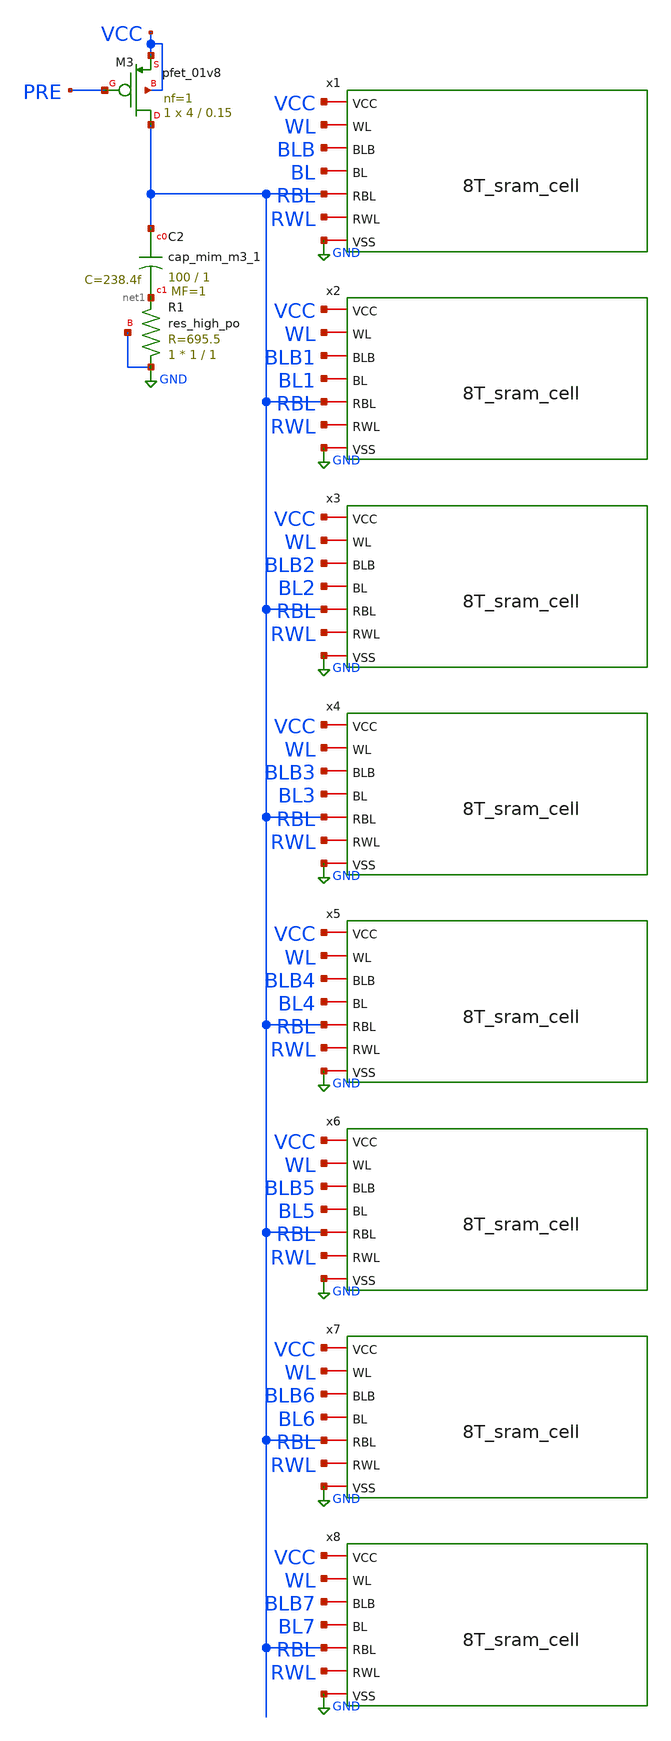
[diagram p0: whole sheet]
** sch_path: vscode/8T_sram_array_test - Copy.sch
**.subckt 8T_sram_array_test - Copy
x1 VCC WL BLB BL RBL RWL GND 8T_sram_cell
XC2 RBL net1 sky130_fd_pr__cap_mim_m3_1 W=100 L=1 MF=1 m=1
XM3 RBL PRE VCC VCC sky130_fd_pr__pfet_01v8 L=0.15 W=4 nf=1 ad='int((1 + 1)/2) * 4 / 1 * 0.29' as='int((1 + 2)/2) * 4 / 1 * 0.29'
+ pd='2*int((1 + 1)/2) * (4 / 1 + 0.29)' ps='2*int((1 + 2)/2) * (4 / 1 + 0.29)' nrd='0.29 / 4 ' nrs='0.29 / 4 '
+ sa=0 sb=0 sd=0 mult=1 m=1
XR1 GND net1 GND sky130_fd_pr__res_high_po W=1 L=1 mult=1 m=1
x2 VCC WL BLB1 BL1 RBL RWL GND 8T_sram_cell
x3 VCC WL BLB2 BL2 RBL RWL GND 8T_sram_cell
x4 VCC WL BLB3 BL3 RBL RWL GND 8T_sram_cell
x5 VCC WL BLB4 BL4 RBL RWL GND 8T_sram_cell
x6 VCC WL BLB5 BL5 RBL RWL GND 8T_sram_cell
x7 VCC WL BLB6 BL6 RBL RWL GND 8T_sram_cell
x8 VCC WL BLB7 BL7 RBL RWL GND 8T_sram_cell
**** begin user architecture code

** opencircuitdesign pdks install
.lib $::SKYWATER_MODELS/sky130.lib.spice tt



.param dly=0ns t_dly=2ns raise=10ps fall=10ps BL_period=20ns prds=128 pre_time=2ns read_time=0.5ns
.param VCC=1.8 VSS=0

V_VCC VCC 0 DC 1.8
V_VSS VSS 0 DC 0
**vss vss 0 DC 0
* PULSE(VSS 1.8 2ns 100ps 100ps 3ns 5ns 4)PULSE(0 1.7 {dly + t_dly/2} {raise} {fall} {(BL_period/2)- t_dly}
*+ {BL_period/2} {prds*2})

V_WL WL 0 PULSE({VSS} {VCC} {dly + t_dly/2} {raise} {fall} {(BL_period/2)- t_dly} {BL_period} {prds*2})


V_BL BLB 0 PULSE({VSS} {VCC} {dly} {raise} {fall} {BL_period} {BL_period*2} {prds})
V_BLB BL 0 PULSE({VCC} {VSS} {dly} {raise} {fall} {BL_period} {BL_period*2} {prds})

V_BL1 BLB1 0 PULSE({VSS} {VCC} {dly} {raise} {fall} {BL_period*2} {BL_period*4} {prds})
V_BLB1 BL1 0 PULSE({VCC} {VSS} {dly} {raise} {fall} {BL_period*2} {BL_period*4} {prds})

V_BL2 BLB2 0 PULSE({VSS} {VCC} {dly} {raise} {fall} {BL_period*4} {BL_period*8} {prds})
V_BLB2 BL2 0 PULSE({VCC} {VSS} {dly} {raise} {fall} {BL_period*4} {BL_period*8} {prds})

V_BL3 BLB3 0 PULSE({VSS} {VCC} {dly} {raise} {fall} {BL_period*8} {BL_period*16} {prds})
V_BLB3 BL3 0 PULSE({VCC} {VSS} {dly} {raise} {fall} {BL_period*8} {BL_period*16} {prds})

V_BL4 BLB4 0 PULSE({VSS} {VCC} {dly} {raise} {fall} {BL_period*16} {BL_period*32} {prds})
V_BLB4 BL4 0 PULSE({VCC} {VSS} {dly} {raise} {fall} {BL_period*16} {BL_period*32} {prds})

V_BL5 BLB5 0 PULSE({VSS} {VCC} {dly} {raise} {fall} {BL_period*32} {BL_period*64} {prds})
V_BLB5 BL5 0 PULSE({VCC} {VSS} {dly} {raise} {fall} {BL_period*32} {BL_period*64} {prds})

V_BL6 BLB6 0 PULSE({VSS} {VCC} {dly} {raise} {fall} {BL_period*64} {BL_period*128} {prds})
V_BLB6 BL6 0 PULSE({VCC} {VSS} {dly} {raise} {fall} {BL_period*64} {BL_period*128} {prds})

V_BL7 BLB7 0 PULSE({VSS} {VCC} {dly} {raise} {fall} {BL_period*128} {BL_period*256} {prds})
V_BLB7 BL7 0 PULSE({VCC} {VSS} {dly} {raise} {fall} {BL_period*128} {BL_period*256} {prds})


V_RWL RWL 0 PULSE({VSS} {VCC} {dly + BL_period/2 + 6ns} {raise} {fall} {read_time} {BL_period} {prds*2})
V_PRE PRE 0 PULSE({VCC} {VSS} {dly + BL_period/2} {raise} {fall} {pre_time} {BL_period} {prds*2})

.tran 0.01ns 5130ns
.control
run
* plot WL BL-2 BLB-4 RWL-6 RBL-8 PRE-10
plot WL BL-2 BL1-4 BL2-6 BL3-8 RWL-10 RBL-12 PRE-14
.endc
.save V(WL) V(BL) V(BL1) V(BL2) V(BL3) V(BL4) V(BL5) V(BL6) V(BL7) V(RWL) V(RBL) V(PRE)



**** end user architecture code
**.ends

* expanding   symbol:  8T_sram_cell.sym # of pins=7
** sym_path: vscode/8T_sram_cell.sym
** sch_path: vscode/8T_sram_cell.sch
.subckt 8T_sram_cell VCC WL BLB BL RBL RWL VSS
*.iopin VCC
*.iopin BLB
*.iopin WL
*.iopin BL
*.iopin VSS
*.iopin RBL
*.iopin RWL
XM1 q_bar q VSS VSS sky130_fd_pr__nfet_01v8 L=0.15 W=1 nf=1 ad='int((1 + 1)/2) * 1 / 1 * 0.29' as='int((1 + 2)/2) * 1 / 1 * 0.29'
+ pd='2*int((1 + 1)/2) * (1 / 1 + 0.29)' ps='2*int((1 + 2)/2) * (1 / 1 + 0.29)' nrd='0.29 / 1 ' nrs='0.29 / 1 '
+ sa=0 sb=0 sd=0 mult=1 m=1
XM2 q q_bar VSS VSS sky130_fd_pr__nfet_01v8 L=0.15 W=1 nf=1 ad='int((1 + 1)/2) * 1 / 1 * 0.29' as='int((1 + 2)/2) * 1 / 1 * 0.29'
+ pd='2*int((1 + 1)/2) * (1 / 1 + 0.29)' ps='2*int((1 + 2)/2) * (1 / 1 + 0.29)' nrd='0.29 / 1 ' nrs='0.29 / 1 '
+ sa=0 sb=0 sd=0 mult=1 m=1
XM3 q_bar q VCC VCC sky130_fd_pr__pfet_01v8 L=0.15 W=4 nf=1 ad='int((1 + 1)/2) * 4 / 1 * 0.29' as='int((1 + 2)/2) * 4 / 1 * 0.29'
+ pd='2*int((1 + 1)/2) * (4 / 1 + 0.29)' ps='2*int((1 + 2)/2) * (4 / 1 + 0.29)' nrd='0.29 / 4 ' nrs='0.29 / 4 '
+ sa=0 sb=0 sd=0 mult=1 m=1
XM4 q q_bar VCC VCC sky130_fd_pr__pfet_01v8 L=0.15 W=4 nf=1 ad='int((1 + 1)/2) * 4 / 1 * 0.29' as='int((1 + 2)/2) * 4 / 1 * 0.29'
+ pd='2*int((1 + 1)/2) * (4 / 1 + 0.29)' ps='2*int((1 + 2)/2) * (4 / 1 + 0.29)' nrd='0.29 / 4 ' nrs='0.29 / 4 '
+ sa=0 sb=0 sd=0 mult=1 m=1
XM5 BLB WL q_bar VSS sky130_fd_pr__nfet_01v8 L=0.15 W=1 nf=1 ad='int((1 + 1)/2) * 1 / 1 * 0.29' as='int((1 + 2)/2) * 1 / 1 * 0.29'
+ pd='2*int((1 + 1)/2) * (1 / 1 + 0.29)' ps='2*int((1 + 2)/2) * (1 / 1 + 0.29)' nrd='0.29 / 1 ' nrs='0.29 / 1 '
+ sa=0 sb=0 sd=0 mult=1 m=1
XM8 q WL BL VSS sky130_fd_pr__nfet_01v8 L=0.15 W=1 nf=1 ad='int((1 + 1)/2) * 1 / 1 * 0.29' as='int((1 + 2)/2) * 1 / 1 * 0.29'
+ pd='2*int((1 + 1)/2) * (1 / 1 + 0.29)' ps='2*int((1 + 2)/2) * (1 / 1 + 0.29)' nrd='0.29 / 1 ' nrs='0.29 / 1 '
+ sa=0 sb=0 sd=0 mult=1 m=1
XM6 net1 q_bar VSS VSS sky130_fd_pr__nfet_01v8 L=0.15 W=1 nf=1 ad='int((1 + 1)/2) * 1 / 1 * 0.29' as='int((1 + 2)/2) * 1 / 1 * 0.29'
+ pd='2*int((1 + 1)/2) * (1 / 1 + 0.29)' ps='2*int((1 + 2)/2) * (1 / 1 + 0.29)' nrd='0.29 / 1 ' nrs='0.29 / 1 '
+ sa=0 sb=0 sd=0 mult=1 m=1
XM7 RBL RWL net1 VSS sky130_fd_pr__nfet_01v8 L=0.15 W=1 nf=1 ad='int((1 + 1)/2) * 1 / 1 * 0.29' as='int((1 + 2)/2) * 1 / 1 * 0.29'
+ pd='2*int((1 + 1)/2) * (1 / 1 + 0.29)' ps='2*int((1 + 2)/2) * (1 / 1 + 0.29)' nrd='0.29 / 1 ' nrs='0.29 / 1 '
+ sa=0 sb=0 sd=0 mult=1 m=1
.ends

.GLOBAL GND
.end
